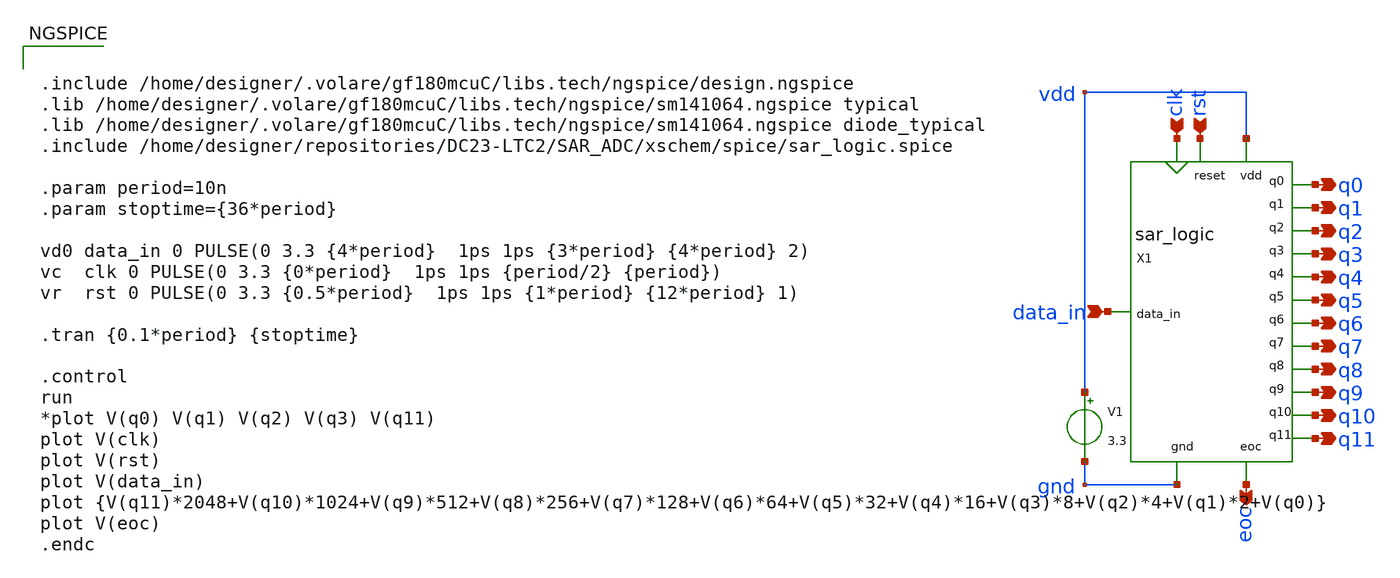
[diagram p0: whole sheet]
** sch_path: SAR_ADC/xschem/test/tb_sar_logic.sch
**.subckt tb_sar_logic eoc data_in clk rst q0 q1 q2 q3 q4 q5 q6 q7 q8 q9 q10 q11
*.opin eoc
*.ipin data_in
*.ipin clk
*.ipin rst
*.opin q0
*.opin q1
*.opin q2
*.opin q3
*.opin q4
*.opin q5
*.opin q6
*.opin q7
*.opin q8
*.opin q9
*.opin q10
*.opin q11
X1 q11 data_in rst clk eoc vdd gnd q10 q9 q8 q7 q6 q5 q4 q3 q2 q1 q0 sar_logic
V1 vdd gnd 3.3
**** begin user architecture code


.include /home/designer/.volare/gf180mcuC/libs.tech/ngspice/design.ngspice
.lib /home/designer/.volare/gf180mcuC/libs.tech/ngspice/sm141064.ngspice typical
.lib /home/designer/.volare/gf180mcuC/libs.tech/ngspice/sm141064.ngspice diode_typical
.include /home/designer/repositories/DC23-LTC2/SAR_ADC/xschem/spice/sar_logic.spice

.param period=10n
.param stoptime={36*period}

vd0 data_in 0 PULSE(0 3.3 {4*period}  1ps 1ps {3*period} {4*period} 2)
vc  clk 0 PULSE(0 3.3 {0*period}  1ps 1ps {period/2} {period})
vr  rst 0 PULSE(0 3.3 {0.5*period}  1ps 1ps {1*period} {12*period} 1)

.tran {0.1*period} {stoptime}

.control
run
*plot V(q0) V(q1) V(q2) V(q3) V(q11)
plot V(clk)
plot V(rst)
plot V(data_in)
plot {V(q11)*2048+V(q10)*1024+V(q9)*512+V(q8)*256+V(q7)*128+V(q6)*64+V(q5)*32+V(q4)*16+V(q3)*8+V(q2)*4+V(q1)*2+V(q0)}
plot V(eoc)
.endc


**** end user architecture code
**.ends

* expanding   symbol:  ../spice/sar_logic.sym # of pins=18
** sym_path: SAR_ADC/xschem/spice/sar_logic.sym
** sch_path: SAR_ADC/xschem/spice/sar_logic.sch
.subckt sar_logic q11 data_in reset clock eoc vdd gnd q10 q9 q8 q7 q6 q5 q4 q3 q2 q1 q0
*.opin q11
*.opin eoc
*.ipin clock
*.ipin data_in
*.ipin reset
*.ipin gnd
*.ipin vdd
*.opin q10
*.opin q9
*.opin q8
*.opin q7
*.opin q6
*.opin q5
*.opin q4
*.opin q3
*.opin q2
*.opin q1
*.opin q0
XFF0 eoc clock reset gnd net14 gnd vdd ff
XFF1 net14 clock vdd reset net1 gnd vdd ff
XFF2 net1 clock vdd reset net2 gnd vdd ff
XFF14 data_in q10 net1 reset q11 gnd vdd ff
XFF3 net2 clock vdd reset net3 gnd vdd ff
XFF15 data_in q9 net2 reset q10 gnd vdd ff
XFF4 net3 clock vdd reset net4 gnd vdd ff
XFF16 data_in q8 net3 reset q9 gnd vdd ff
XFF17 data_in q7 net4 reset q8 gnd vdd ff
XFF5 net4 clock vdd reset net5 gnd vdd ff
XFF18 data_in q6 net5 reset q7 gnd vdd ff
XFF19 data_in q5 net6 reset q6 gnd vdd ff
XFF6 net5 clock vdd reset net6 gnd vdd ff
XFF7 net6 clock vdd reset net7 gnd vdd ff
XFF8 net7 clock vdd reset net8 gnd vdd ff
XFF9 net8 clock vdd reset net9 gnd vdd ff
XFF20 data_in q4 net7 reset q5 gnd vdd ff
XFF21 data_in q3 net8 reset q4 gnd vdd ff
XFF22 data_in q2 net9 reset q3 gnd vdd ff
XFF23 data_in q1 net10 reset q2 gnd vdd ff
XFF10 net9 clock vdd reset net10 gnd vdd ff
XFF11 net10 clock vdd reset net11 gnd vdd ff
XFF12 net11 clock vdd reset net12 gnd vdd ff
XFF24 data_in q0 net11 reset q1 gnd vdd ff
XFF13 net12 clock vdd reset eoc gnd vdd ff
XFF25 data_in net13 net12 reset q0 gnd vdd ff
XFF26 gnd gnd eoc reset net13 gnd vdd ff
.ends


* expanding   symbol:  /foss/designs/sar_adc/xschem/spice/ff.sym # of pins=7
** sym_path: SAR_ADC/xschem/spice/ff.sym
** sch_path: SAR_ADC/xschem/spice/ff.sch
.subckt ff data_in clock set reset data_out gnd vdd
*.ipin data_in
*.ipin clock
*.ipin vdd
*.ipin gnd
*.opin data_out
*.ipin set
*.ipin reset
XFF1 net2 net3 net4 clock net1 vdd gnd gnd gnd gf180mcu_fd_sc_mcu7t5v0__dffrsnq_1
x1 vdd gnd net2 data_in inv cl=0.28u wp=0.44u wn=0.22u
x2 vdd gnd net4 reset inv cl=0.28u wp=0.44u wn=0.22u
x3 vdd gnd net3 set inv cl=0.28u wp=0.44u wn=0.22u
x4 vdd gnd data_out net1 inv cl=0.28u wp=0.44u wn=0.22u
.ends


* expanding   symbol:  /foss/designs/sar_adc/xschem/spice/inv.sym # of pins=4
** sym_path: SAR_ADC/xschem/spice/inv.sym
** sch_path: SAR_ADC/xschem/spice/inv.sch
.subckt inv vdd gnd vout vin  cl=0.28u wp=0.44u wn=0.22u
*.ipin gnd
*.ipin vdd
*.ipin vin
*.opin vout
XM1 gnd vin vout gnd nfet_03v3 L=0.28u W=4u nf=1 ad='int((nf+1)/2) * W/nf * 0.18u' as='int((nf+2)/2) * W/nf * 0.18u'
+ pd='2*int((nf+1)/2) * (W/nf + 0.18u)' ps='2*int((nf+2)/2) * (W/nf + 0.18u)' nrd='0.18u / W' nrs='0.18u / W'
+ sa=0 sb=0 sd=0 m=1
XM2 vdd vin vout vdd pfet_03v3 L=0.28u W=4u nf=1 ad='int((nf+1)/2) * W/nf * 0.18u' as='int((nf+2)/2) * W/nf * 0.18u'
+ pd='2*int((nf+1)/2) * (W/nf + 0.18u)' ps='2*int((nf+2)/2) * (W/nf + 0.18u)' nrd='0.18u / W' nrs='0.18u / W'
+ sa=0 sb=0 sd=0 m=1
.ends

.end
